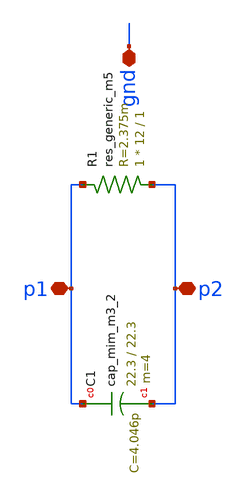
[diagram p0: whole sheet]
** sch_path: examples/sq_1nH_2.5GHz/xschem/lc-lvs.sch
**.subckt lc-lvs p1 p2 gnd
*.iopin p1
*.iopin p2
*.iopin gnd
XC1 p1 p2 sky130_fd_pr__cap_mim_m3_2 W=22.3 L=22.3 MF=4 m=4
R1 p2 p1 sky130_fd_pr__res_generic_m5 W=12 L=1 m=1
**.ends
.end
